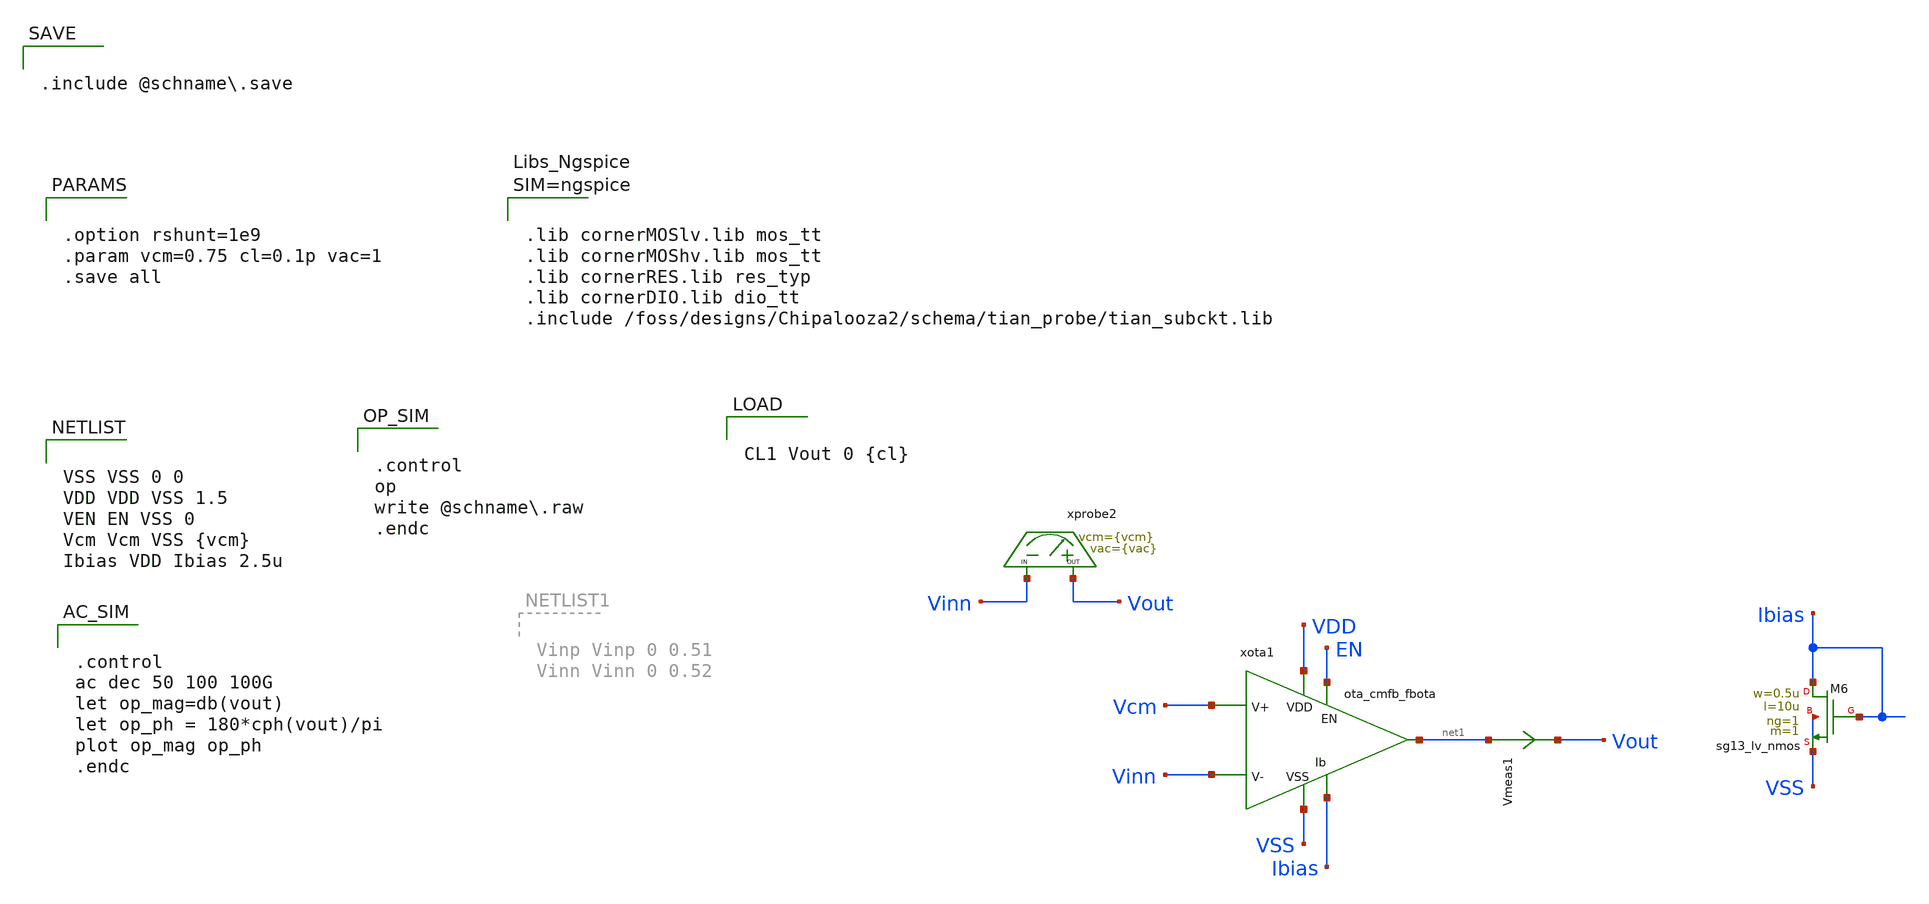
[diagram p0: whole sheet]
** sch_path: schema/ota_cmfb_fbota/ota_cmfb_fbota_tb.sch
**.subckt ota_cmfb_fbota_tb
Vmeas1 net1 Vout 0
.save i(vmeas1)
xprobe2 Vout Vinn ac_probe vcm={vcm} vac={vac}
xota1 VDD EN Ibias Vinn Vcm net1 VSS ota_cmfb_fbota
XM6 Ibias Ibias VSS VSS sg13_lv_nmos w=0.5u l=10u ng=1 m=1 mm_ok=1
**** begin user architecture code


VSS VSS 0 0
VDD VDD VSS 1.5
VEN EN VSS 0
Vcm Vcm VSS {vcm}
Ibias VDD Ibias 2.5u



.control
op
write @schname.raw
.endc




.lib cornerMOSlv.lib mos_tt
.lib cornerMOShv.lib mos_tt
.lib cornerRES.lib res_typ
.lib cornerDIO.lib dio_tt
.include /foss/designs/Chipalooza2/schema/tian_probe/tian_subckt.lib





.control
ac dec 50 100 100G
let op_mag=db(vout)
let op_ph = 180*cph(vout)/pi
plot op_mag op_ph
.endc




.option rshunt=1e9
.param vcm=0.75 cl=0.1p vac=1
.save all




CL1 Vout 0 {cl}



.include @schname.save

**** end user architecture code
**.ends

* expanding   symbol:  /foss/designs/Chipalooza2/schema/ac_probe/ac_probe.sym # of pins=2
** sym_path: schema/ac_probe/ac_probe.sym
** sch_path: schema/ac_probe/ac_probe.sch
.subckt ac_probe OUT IN  vcm=0.75 vac=0.01

*.iopin IN
*.iopin OUT
C1 net1 IN 1 m=1
V1 net1 0 {vcm} ac {vac}
L1 OUT net2 1G m=1
R1 net2 IN 1m m=1
.ends


* expanding   symbol:  /foss/designs/Chipalooza2/schema/ota_cmfb_fbota/ota_cmfb_fbota.sym # of
*+ pins=7
** sym_path: schema/ota_cmfb_fbota/ota_cmfb_fbota.sym
** sch_path: schema/ota_cmfb_fbota/ota_cmfb_fbota.sch
.subckt ota_cmfb_fbota VDD EN Ibias Vinn Vinp Vout VSS
*.opin Vout
*.iopin VDD
*.iopin VSS
*.ipin Vinp
*.ipin Ibias
*.ipin Vinn
*.ipin EN
XM1 Vout mirror VSS VSS sg13_lv_nmos w=0.5u l=10u ng=1 m=2 mm_ok=1
XM2 net1 Vinn Vout VDD sg13_lv_pmos w=2.5u l=1u ng=1 m=2 mm_ok=1
XM3 mirror mirror VSS VSS sg13_lv_nmos w=0.5u l=10u ng=1 m=2 mm_ok=1
XM4 net1 Vinp mirror VDD sg13_lv_pmos w=2.5u l=1u ng=1 m=2 mm_ok=1
XM5 VDD tail_bias net1 VDD sg13_lv_pmos w=2.5u l=5u ng=1 m=4 mm_ok=1
XM7 mirror EN VSS VSS sg13_lv_nmos w=0.15u l=0.13u ng=1 m=1 mm_ok=1
XM8 VDD tail_bias tail_bias VDD sg13_lv_pmos w=2.5u l=5u ng=1 m=1 mm_ok=1
XM9 tail_bias Ibias VSS VSS sg13_lv_nmos w=0.5u l=10u ng=1 m=1 mm_ok=1
.ends

.end
